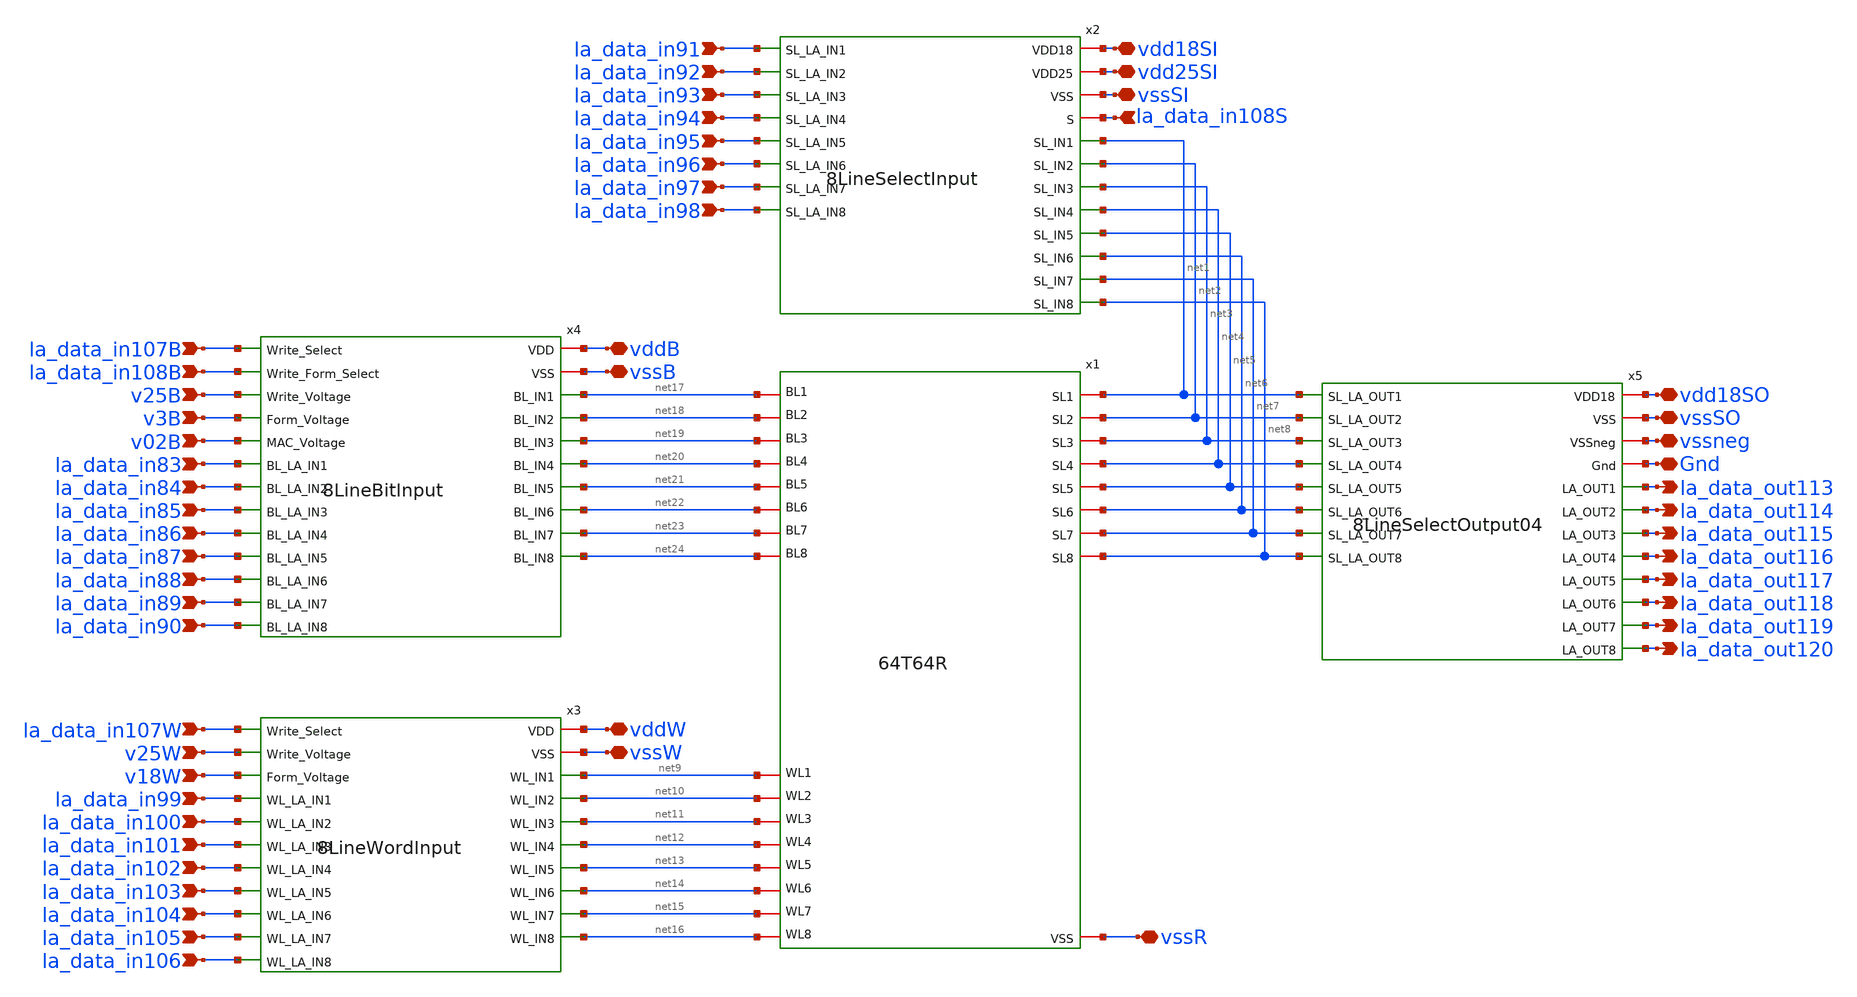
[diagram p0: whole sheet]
** sch_path: xschem/04Compute.sch
**.subckt 04Compute la_data_in91 la_data_in98 la_data_in92 la_data_in93 la_data_in97 la_data_in96
*+ la_data_in95 la_data_in94 la_data_in83 la_data_in84 la_data_in85 la_data_in86 la_data_in87 la_data_in88
*+ la_data_in89 la_data_in90 la_data_in99 la_data_in100 la_data_in101 la_data_in102 la_data_in103 la_data_in104
*+ la_data_in105 la_data_in106 la_data_in107B la_data_in107W la_data_in108B la_data_in108S v25B v3B v02B v25W v18W
*+ vddB vssB vssW vddW vssR vdd18SI vdd25SI vssSI vdd18SO vssSO Gnd vssneg la_data_out113 la_data_out114
*+ la_data_out115 la_data_out116 la_data_out117 la_data_out118 la_data_out119 la_data_out120
*.ipin la_data_in91
*.ipin la_data_in98
*.ipin la_data_in92
*.ipin la_data_in93
*.ipin la_data_in97
*.ipin la_data_in96
*.ipin la_data_in95
*.ipin la_data_in94
*.ipin la_data_in83
*.ipin la_data_in84
*.ipin la_data_in85
*.ipin la_data_in86
*.ipin la_data_in87
*.ipin la_data_in88
*.ipin la_data_in89
*.ipin la_data_in90
*.ipin la_data_in99
*.ipin la_data_in100
*.ipin la_data_in101
*.ipin la_data_in102
*.ipin la_data_in103
*.ipin la_data_in104
*.ipin la_data_in105
*.ipin la_data_in106
*.ipin la_data_in107B
*.ipin la_data_in107W
*.ipin la_data_in108B
*.ipin la_data_in108S
*.ipin v25B
*.ipin v3B
*.ipin v02B
*.ipin v25W
*.ipin v18W
*.iopin vddB
*.iopin vssB
*.iopin vssW
*.iopin vddW
*.iopin vssR
*.iopin vdd18SI
*.iopin vdd25SI
*.iopin vssSI
*.iopin vdd18SO
*.iopin vssSO
*.iopin Gnd
*.iopin vssneg
*.opin la_data_out113
*.opin la_data_out114
*.opin la_data_out115
*.opin la_data_out116
*.opin la_data_out117
*.opin la_data_out118
*.opin la_data_out119
*.opin la_data_out120
x1 net9 net10 net11 net12 vssR net13 net14 net15 net16 net21 net7 net20 net19 net22 net5 net4 net3
+ net2 net1 net24 net23 net6 net18 net8 net17 64T64R
x2 vdd18SI vdd25SI vssSI la_data_in91 la_data_in108S net1 la_data_in92 net2 la_data_in93 net3
+ la_data_in94 net4 la_data_in95 net5 la_data_in96 net6 la_data_in97 net7 la_data_in98 net8 8LineSelectInput
x3 la_data_in107W v25W v18W vddW vssW la_data_in99 net9 la_data_in100 net10 la_data_in101 net11
+ la_data_in102 net12 la_data_in103 net13 la_data_in104 net14 la_data_in105 net15 la_data_in106 net16
+ 8LineWordInput
x4 la_data_in107B v25B v3B vddB vssB la_data_in83 la_data_in108B v02B net17 la_data_in84 net18
+ la_data_in85 net19 la_data_in86 net20 la_data_in87 net21 la_data_in88 net22 la_data_in89 net23 la_data_in90
+ net24 8LineBitInput
x5 vdd18SO vssSO vssneg Gnd net1 la_data_out113 net2 la_data_out114 net3 la_data_out115 net4
+ la_data_out116 net5 la_data_out117 net6 la_data_out118 net7 la_data_out119 net8 la_data_out120 8LineSelectOutput04
**.ends
.end
